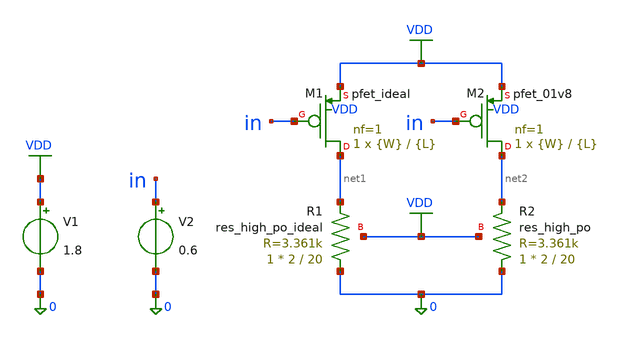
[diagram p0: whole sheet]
** sch_path: designs_backup/designs/lab2/test_M1vsM2.sch
**.subckt test_M1vsM2
XM1 net1 in VDD VDD sky130_fd_pr__pfet_ideal L={L} W={W} nf=1 ad='int((1 + 1)/2) * {W} / 1 * 0.29' as='int((1 + 2)/2) * {W} / 1 * 0.29'
+ pd='2*int((1 + 1)/2) * ({W} / 1 + 0.29)' ps='2*int((1 + 2)/2) * ({W} / 1 + 0.29)' nrd='0.29 / {W} ' nrs='0.29 / {W} '
+ sa=0 sb=0 sd=0 mult=1 m=1
XM2 net2 in VDD VDD sky130_fd_pr__pfet_01v8 L={L} W={W} nf=1 ad='int((1 + 1)/2) * {W} / 1 * 0.29' as='int((1 + 2)/2) * {W} / 1 * 0.29'
+ pd='2*int((1 + 1)/2) * ({W} / 1 + 0.29)' ps='2*int((1 + 2)/2) * ({W} / 1 + 0.29)' nrd='0.29 / {W} ' nrs='0.29 / {W} '
+ sa=0 sb=0 sd=0 mult=1 m=1
XR1 0 net1 VDD sky130_fd_pr__res_high_po_ideal W=2 L=20 mult=1 m=1
XR2 0 net2 VDD sky130_fd_pr__res_high_po W=2 L=20 mult=1 m=1
V1 VDD 0 1.8
V2 in 0 0.6
**** begin user architecture code

** opencircuitdesign pdks install
.lib $::SKYWATER_MODELS/sky130.lib.spice tt

* force include MC files
.include "$::SKYWATER_MODELS/parameters/montecarlo.spice"
.include "$::SKYWATER_MODELS/parameters/critical.spice"

* force mismatch/process params
.param mc_mm_switch = 1
.param mc_pr_switch = 1

* disable pfet_ideal from mismatch/process
.subckt sky130_fd_pr__pfet_ideal D G S B W=0.42 L=0.18
  .param mc_mm_switch=0
  .param mc_pr_switch=0
  XIDEAL D G S B sky130_fd_pr__pfet_01v8 W={W} L={L}
.ends
* disable res_high_po_ideal from mismatch/process
.subckt sky130_fd_pr__res_high_po_ideal r0 r1 b W=2 L=20 mult=1
  .param mc_mm_switch=0
  .param mc_pr_switch=0
  .param l_mult = mult
  XIDEAL r0 r1 b sky130_fd_pr__res_high_po W={W} L={L} mult={l_mult}
.ends



.param mc_runs=100
.options savecurrents
.param W=5
.param L=5
.control
  let runs = 100
  shell mkdir -p /foss/designs/lab2/results/1.8
  shell rm -f /foss/designs/lab2/results/1.8/test_runs.dat
+ /foss/designs/lab2/results/1.8/test_stats.dat
  let i_m1 = vector(runs)
  let i_m2 = vector(runs)
  let i_diff = vector(runs)
  let r = 0
  echo ----- Monte Carlo Current Mismatch Runs ----- >> /foss/designs/lab2/results/1.8/test_runs.dat
  echo ----- Mismatch Statistical Analysis ----- >> /foss/designs/lab2/results/1.8/test_stats.dat
  dowhile r < runs
    reset
    op
    let i_m1[r] = @m.xm1.xideal.msky130_fd_pr__pfet_01v8[id]
    let i_m2[r] = @m.xm2.msky130_fd_pr__pfet_01v8[id]
    let i_diff[r] = i_m1[r] - i_m2[r]
    let cur_m1 = i_m1[r]
    let cur_m2 = i_m2[r]
    let cur_diff = i_diff[r]
    set appendwrite
    echo RUN= $&r I(M1)= $&cur_m1 I(M2)= $&cur_m2 Diff= $&cur_diff >>
+ /foss/designs/lab2/results/1.8/test_runs.dat
    let r = r + 1
  end
  let avg_diff = mean(i_diff)
  let sig_diff = stddev(i_diff)
  let min_diff = minimum(i_diff)
  let max_diff = maximum(i_diff)
  echo MIN_DIFF= $&min_diff MAX_DIFF= $&max_diff AVG_DIFF= $&avg_diff SIGMA_DIFF= $&sig_diff >>
+ /foss/designs/lab2/results/1.8/test_stats.dat
.endc


**** end user architecture code
**.ends
.GLOBAL VDD
.end
